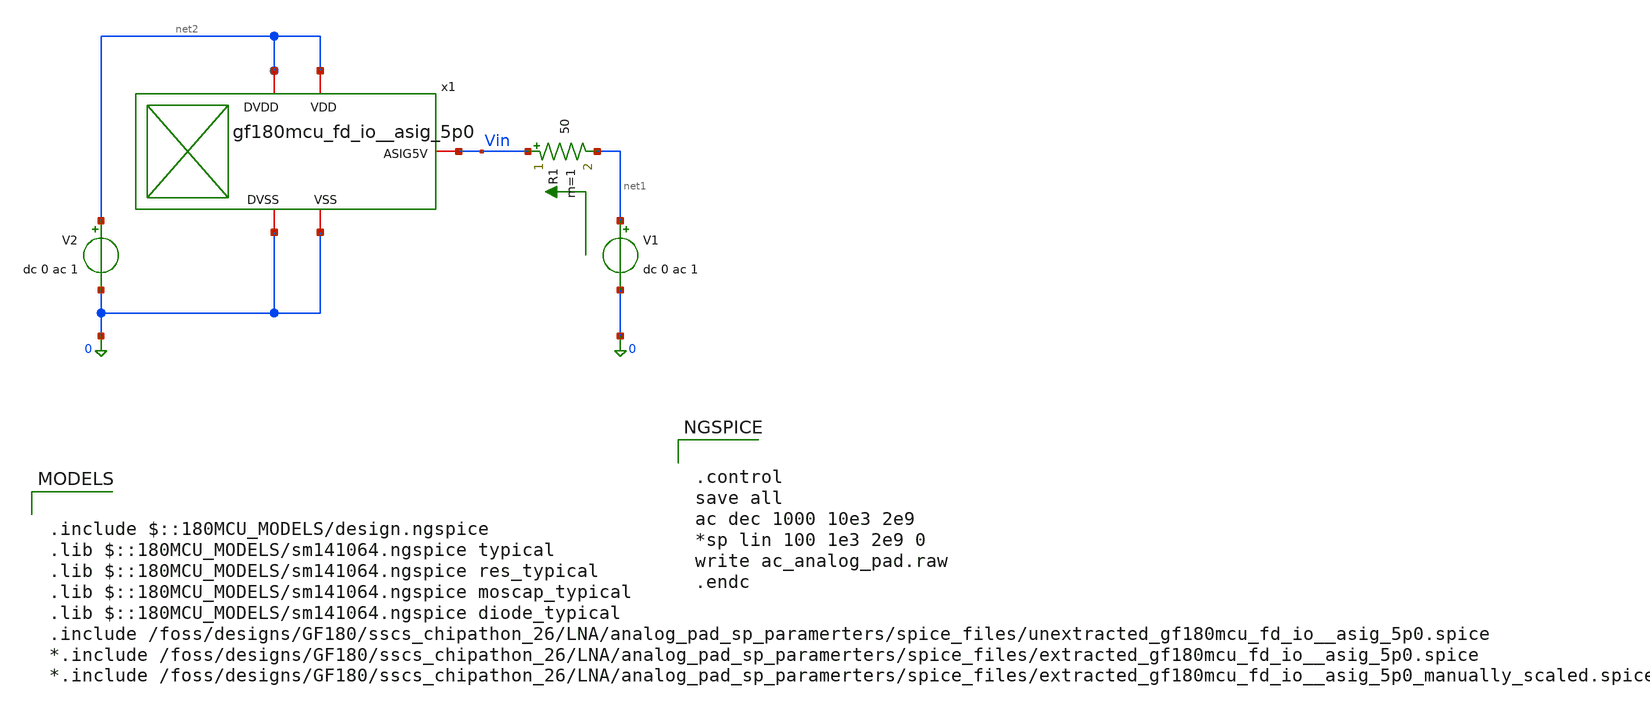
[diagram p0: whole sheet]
** sch_path: analog_pad_sp_paramerters/xschem/schematic_ac.sch
**.subckt schematic_ac
V1 net1 0 dc 0 ac 1
R1 Vin net1 50 m=1
x1 net2 Vin 0 net2 0 gf180mcu_fd_io__asig_5p0
V2 net2 0 dc 0 ac 1
**** begin user architecture code


.control
save all
ac dec 1000 10e3 2e9
*sp lin 100 1e3 2e9 0
write ac_analog_pad.raw
.endc



.include $::180MCU_MODELS/design.ngspice
.lib $::180MCU_MODELS/sm141064.ngspice typical
.lib $::180MCU_MODELS/sm141064.ngspice res_typical
.lib $::180MCU_MODELS/sm141064.ngspice moscap_typical
.lib $::180MCU_MODELS/sm141064.ngspice diode_typical
.include /foss/designs/GF180/sscs_chipathon_26/LNA/analog_pad_sp_paramerters/spice_files/unextracted_gf180mcu_fd_io__asig_5p0.spice
*.include /foss/designs/GF180/sscs_chipathon_26/LNA/analog_pad_sp_paramerters/spice_files/extracted_gf180mcu_fd_io__asig_5p0.spice
*.include /foss/designs/GF180/sscs_chipathon_26/LNA/analog_pad_sp_paramerters/spice_files/extracted_gf180mcu_fd_io__asig_5p0_manually_scaled.spice

**** end user architecture code
**.ends
.end
